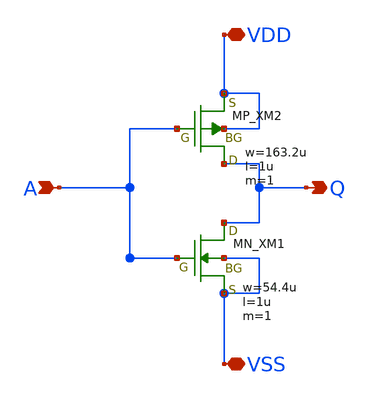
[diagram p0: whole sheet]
** sch_path: member_project/inverter/RISE-A/jijinbei/inverter.sch
**.subckt inverter A Q VSS VDD
*.ipin A
*.opin Q
*.iopin VSS
*.iopin VDD
XXM1 Q A VSS VSS NMOS w=54.4u l=1u nrd=0 nrs=0 m=1
XXM2 Q A VDD VDD PMOS w=163.2u l=1u nrd=0 nrs=0 m=1
**.ends
.end
